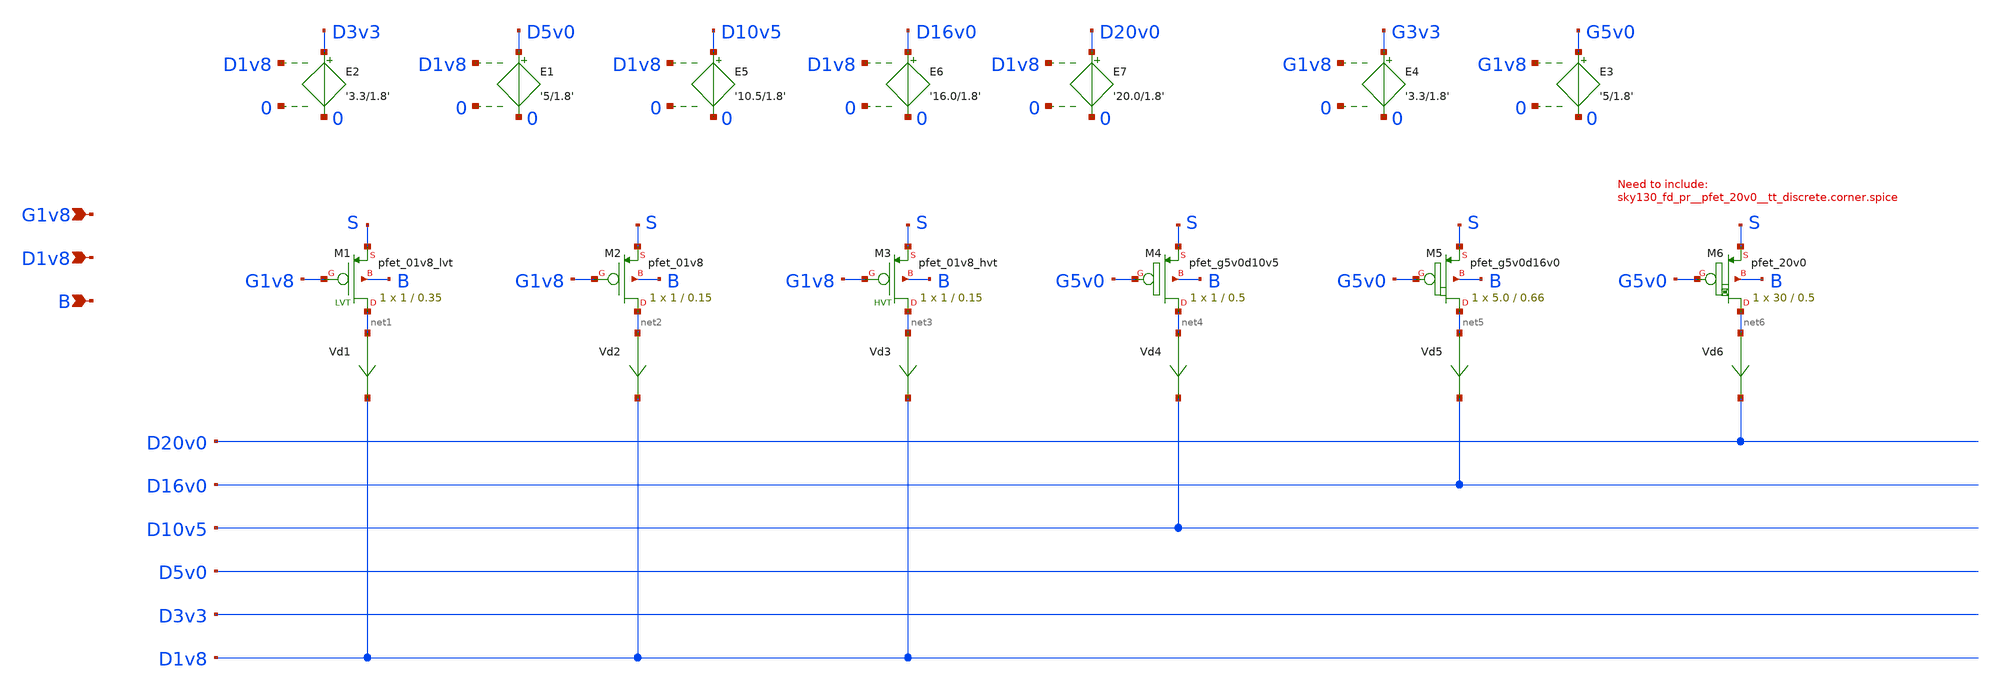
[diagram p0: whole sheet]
** sch_path: sky130_tests/test_pmos.sch
* Copyright 2021 Stefan Frederik Schippers
* Licensed under the Apache License, Version 2.0 (the "License");
* you may not use this file except in compliance with the License.
* You may obtain a copy of the License at
* https://www.apache.org/licenses/LICENSE-2.0
* Unless required by applicable law or agreed to in writing, software
* distributed under the License is distributed on an "AS IS" BASIS,
* WITHOUT WARRANTIES OR CONDITIONS OF ANY KIND, either express or implied.
* See the License for the specific language governing permissions and
* limitations under the License.
**.subckt test_pmos G1v8 D1v8 B
*.ipin G1v8
*.ipin D1v8
*.ipin B
Vd1 net1 D1v8 0
.save i(vd1)
Vd2 net2 D1v8 0
.save i(vd2)
E1 D5v0 0 D1v8 0 '5/1.8'
E2 D3v3 0 D1v8 0 '3.3/1.8'
E3 G5v0 0 G1v8 0 '5/1.8'
E4 G3v3 0 G1v8 0 '3.3/1.8'
E5 D10v5 0 D1v8 0 '10.5/1.8'
Vd3 net3 D1v8 0
.save i(vd3)
XM3 net3 G1v8 S B sky130_fd_pr__pfet_01v8_hvt L=0.15 W=1 nf=1 ad='int((nf+1)/2) * W/nf * 0.29' as='int((nf+2)/2) * W/nf * 0.29'
+ pd='2*int((nf+1)/2) * (W/nf + 0.29)' ps='2*int((nf+2)/2) * (W/nf + 0.29)' nrd='0.29 / W' nrs='0.29 / W'
+ sa=0 sb=0 sd=0 mult=1 m=1
Vd4 net4 D10v5 0
.save i(vd4)
XM4 net4 G5v0 S B sky130_fd_pr__pfet_g5v0d10v5 L=0.5 W=1 nf=1 ad='int((nf+1)/2) * W/nf * 0.29' as='int((nf+2)/2) * W/nf * 0.29'
+ pd='2*int((nf+1)/2) * (W/nf + 0.29)' ps='2*int((nf+2)/2) * (W/nf + 0.29)' nrd='0.29 / W' nrs='0.29 / W'
+ sa=0 sb=0 sd=0 mult=1 m=1
XM1 net1 G1v8 S B sky130_fd_pr__pfet_01v8_lvt L=0.35 W=1 nf=1 ad='int((nf+1)/2) * W/nf * 0.29' as='int((nf+2)/2) * W/nf * 0.29'
+ pd='2*int((nf+1)/2) * (W/nf + 0.29)' ps='2*int((nf+2)/2) * (W/nf + 0.29)' nrd='0.29 / W' nrs='0.29 / W'
+ sa=0 sb=0 sd=0 mult=1 m=1
XM2 net2 G1v8 S B sky130_fd_pr__pfet_01v8 L=0.15 W=1 nf=1 ad='int((nf+1)/2) * W/nf * 0.29' as='int((nf+2)/2) * W/nf * 0.29'
+ pd='2*int((nf+1)/2) * (W/nf + 0.29)' ps='2*int((nf+2)/2) * (W/nf + 0.29)' nrd='0.29 / W' nrs='0.29 / W'
+ sa=0 sb=0 sd=0 mult=1 m=1
Vd5 net5 D16v0 0
.save i(vd5)
XM5 net5 G5v0 S B sky130_fd_pr__pfet_g5v0d16v0 L=0.66 W=5.0 nf=1 ad='int((nf+1)/2) * W/nf * 0.29' as='int((nf+2)/2) * W/nf * 0.29'
+ pd='2*int((nf+1)/2) * (W/nf + 0.29)' ps='2*int((nf+2)/2) * (W/nf + 0.29)' nrd='0.29 / W' nrs='0.29 / W'
+ sa=0 sb=0 sd=0 mult=1 m=1
E6 D16v0 0 D1v8 0 '16.0/1.8'
E7 D20v0 0 D1v8 0 '20.0/1.8'
XM6 net6 G5v0 S B sky130_fd_pr__pfet_20v0 L=0.5 W=30 m=1
Vd6 net6 D20v0 0
.save i(vd6)
**** begin user architecture code


vg G1v8 0 0
vs s 0 0
vd D1v8 0 0
vb b 0 0
.control
save all
dc vd 0 -1.8 -0.01 vg 0 -1.8 -0.2
plot all.vd1#branch vs D1v8
plot all.vd2#branch vs D1v8
plot all.vd3#branch vs D1v8
plot all.vd4#branch vs D10v5
plot all.vd5#branch vs D16v0
plot all.vd6#branch vs D20v0
.endc


 ** manual skywater pdks install (with patches applied)
* .lib $::SKYWATER_MODELS/models/sky130.lib.spice tt

** opencircuitdesign pdks install
.lib $::SKYWATER_MODELS/sky130.lib.spice tt

.param mc_mm_switch=0
.param mc_pr_switch=0


** manual skywater-pdk install (with patches applied).
* .include $::SKYWATER_MODELS/cells/pfet_20v0/sky130_fd_pr__pfet_20v0__tt_discrete.corner.spice

** opencircuitdesign pdks install
.include $::SKYWATER_MODELS/../../libs.ref/sky130_fd_pr/spice/sky130_fd_pr__pfet_20v0__tt_discrete.corner.spice

**** end user architecture code
**.ends
.end
